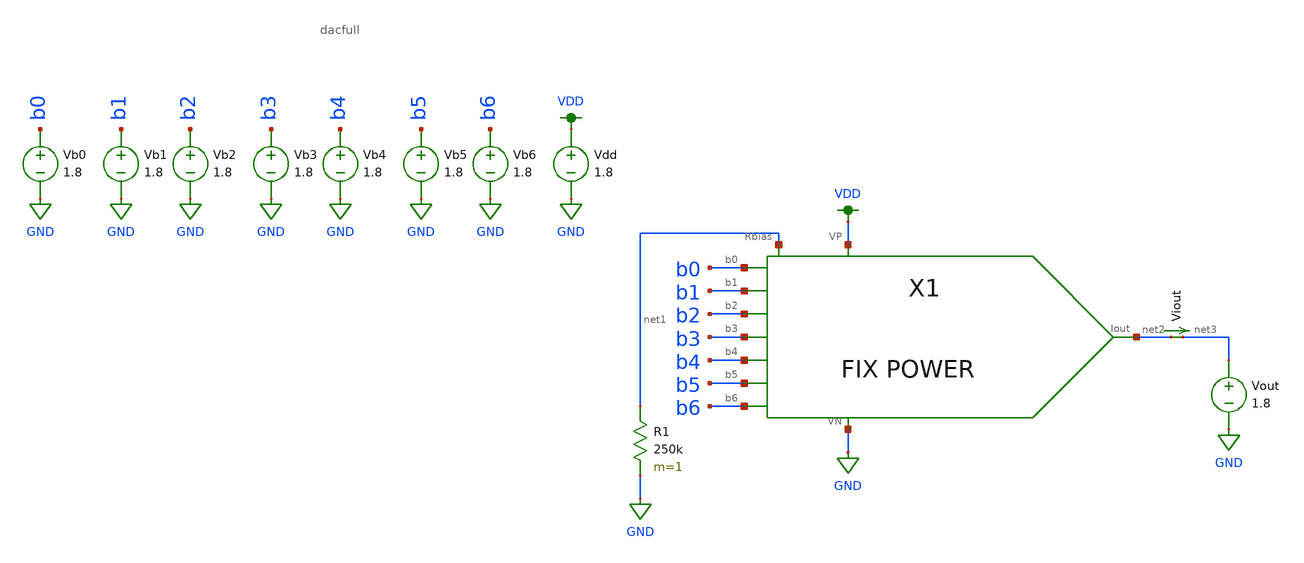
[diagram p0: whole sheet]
** sch_path: design-files/dac_harness_varied_output.sch
**.subckt dac_harness_varied_output
X1 VDD b0 b1 b2 b3 b4 b5 b6 GND net2 net1 dacfull
Vb0 b0 GND 1.8
Vb1 b1 GND 1.8
Vb2 b2 GND 1.8
Vb3 b3 GND 1.8
Vb4 b4 GND 1.8
Vb5 b5 GND 1.8
Vb6 b6 GND 1.8
Vdd VDD GND 1.8
R1 net1 GND 250k m=1
Viout net2 net3 0
.save i(viout)
Vout net3 GND 1.8
**** begin user architecture code

.dc Vout 0 1.8 0.01
.save i(Viout)


.option wnflag=1
.param MC_SWITCH=1
.lib ~/skywater/skywater-pdk/libraries/sky130_fd_pr_ngspice/latest/models/sky130.lib.spice tt

**** end user architecture code
**.ends
.GLOBAL GND
.GLOBAL VDD
.end
